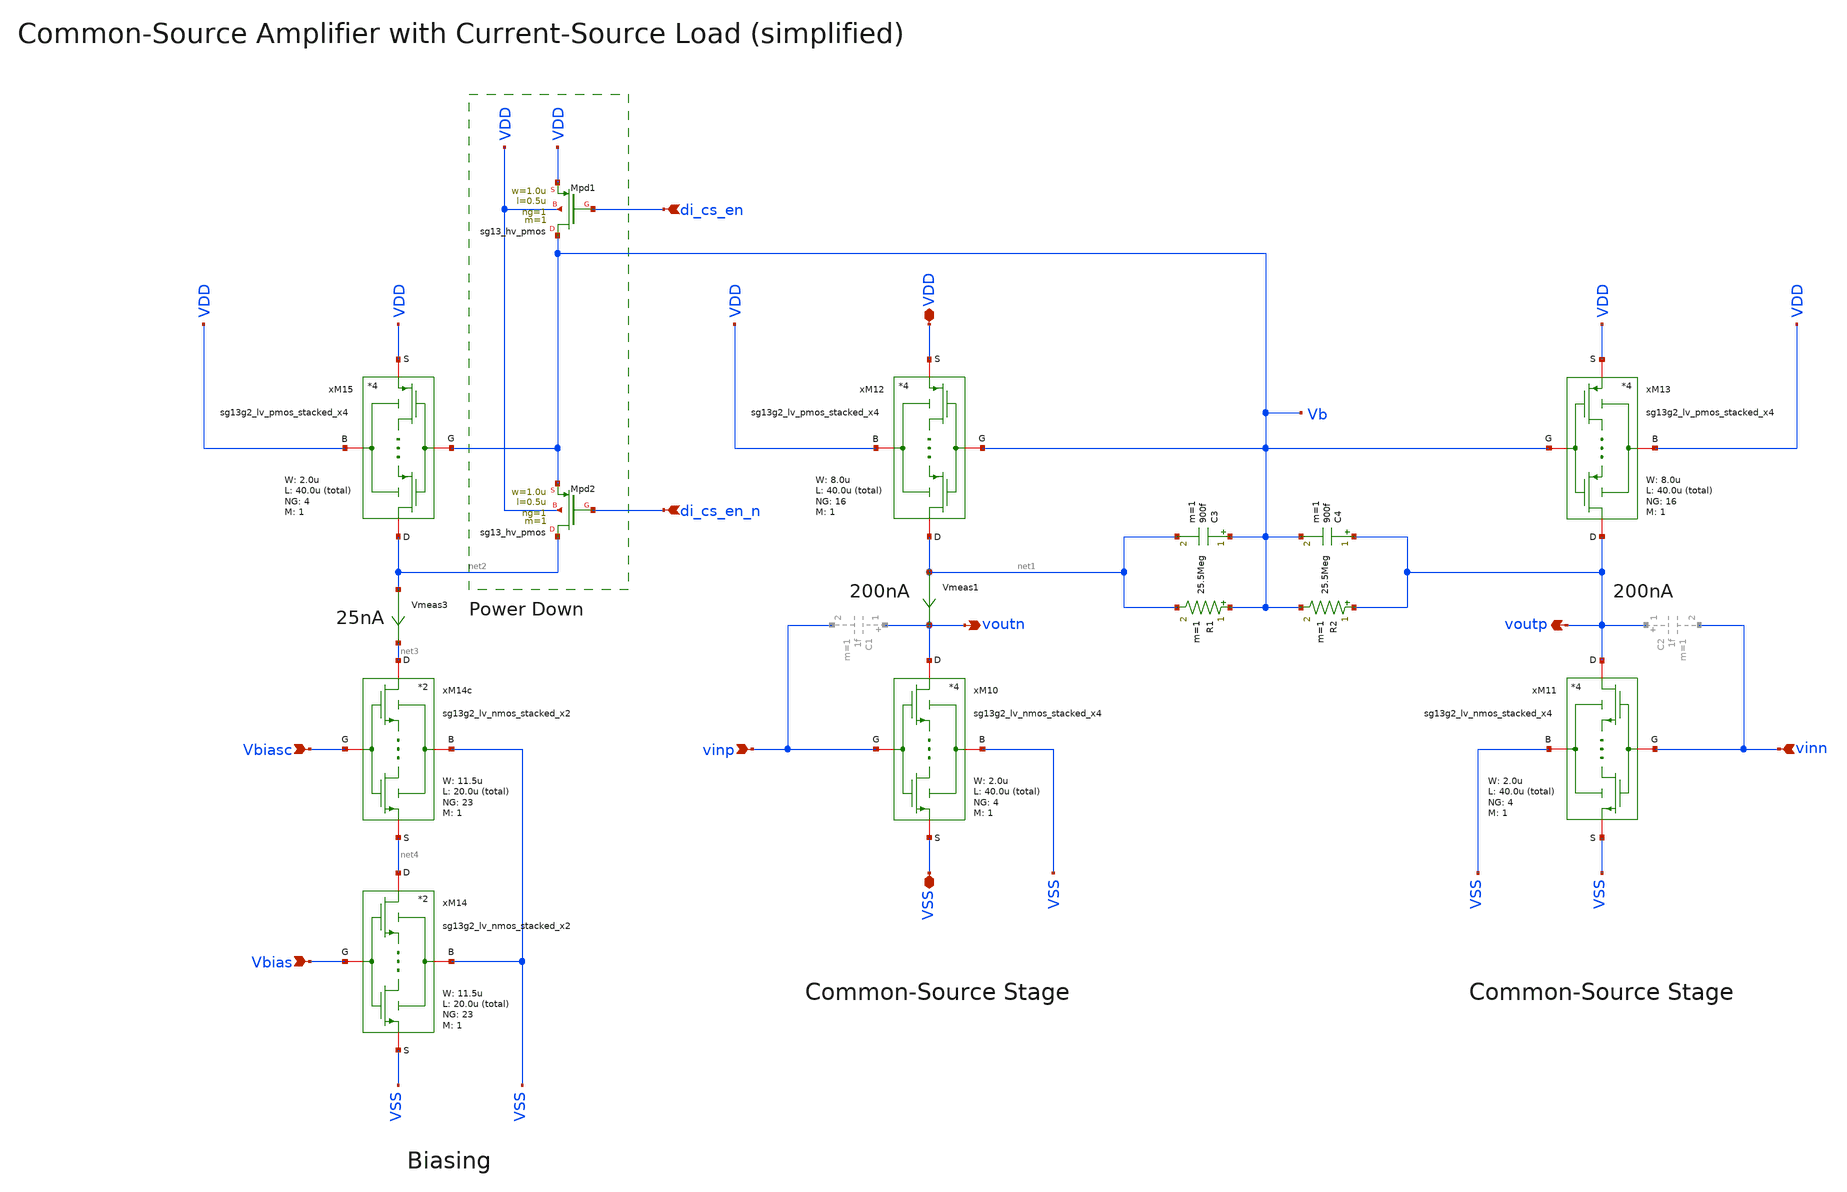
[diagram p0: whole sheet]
** sch_path: SG13G2_ATBS-ADC-main/xschem/bio_amplifier/amplifier_core/common_source_amplifier/common_source_amplifier_simplified.sch
**.subckt common_source_amplifier_simplified vinp vinn voutp voutn VDD VSS di_cs_en di_cs_en_n Vbias
*+ Vbiasc
*.ipin vinp
*.ipin vinn
*.opin voutp
*.opin voutn
*.iopin VDD
*.iopin VSS
*.ipin di_cs_en
*.ipin di_cs_en_n
*.ipin Vbias
*.ipin Vbiasc
xM12 net1 Vb VDD VDD sg13g2_lv_pmos_stacked_x4 W_P=8.0u L_P=40.0u NG_P=16 M_P=1
xM10 voutn vinp VSS VSS sg13g2_lv_nmos_stacked_x4 W_N=2.0u L_N=40.0u NG_N=4 M_N=1
R1 Vb net1 25.5Meg m=1
C3 Vb net1 900f m=1
xM13 voutp Vb VDD VDD sg13g2_lv_pmos_stacked_x4 W_P=8.0u L_P=40.0u NG_P=16 M_P=1
xM11 voutp vinn VSS VSS sg13g2_lv_nmos_stacked_x4 W_N=2.0u L_N=40.0u NG_N=4 M_N=1
C4 voutp Vb 900f m=1
R2 voutp Vb 25.5Meg m=1
xM15 net2 Vb VDD VDD sg13g2_lv_pmos_stacked_x4 W_P=2.0u L_P=40.0u NG_P=4 M_P=1
Vmeas1 net1 voutn 0
.save i(vmeas1)
XMpd2 net2 di_cs_en_n Vb VDD sg13_hv_pmos w=1.0u l=0.5u ng=1 m=1 mm_ok=1
XMpd1 Vb di_cs_en VDD VDD sg13_hv_pmos w=1.0u l=0.5u ng=1 m=1 mm_ok=1
Vmeas3 net2 net3 0
.save i(vmeas3)
xM14c net3 Vbiasc VSS net4 sg13g2_lv_nmos_stacked_x2 W_N=11.5u L_N=20.0u NG_N=23 M_N=1
xM14 net4 Vbias VSS VSS sg13g2_lv_nmos_stacked_x2 W_N=11.5u L_N=20.0u NG_N=23 M_N=1
**.ends

* expanding   symbol:  stacked_transistors/sg13g2_lv_pmos_stacked/sg13g2_lv_pmos_stacked_x4.sym # of
*+ pins=4
** sym_path: SG13G2_ATBS-ADC-main/xschem/stacked_transistors/sg13g2_lv_pmos_stacked/sg13g2_lv_pmos_stacked_x4.sym
** sch_path: SG13G2_ATBS-ADC-main/xschem/stacked_transistors/sg13g2_lv_pmos_stacked/sg13g2_lv_pmos_stacked_x4.sch
.subckt sg13g2_lv_pmos_stacked_x4 D G B S  W_P=1.0u L_P=0.45u NG_P=1 M_P=1
*.iopin D
*.iopin S
*.iopin G
*.iopin B
XM1 net1 G S B sg13_lv_pmos w=W_P l=L_P/4 ng=NG_P m=M_P mm_ok=1
XM2 net3 G net1 B sg13_lv_pmos w=W_P l=L_P/4 ng=NG_P m=M_P mm_ok=1
XM3 net2 G net3 B sg13_lv_pmos w=W_P l=L_P/4 ng=NG_P m=M_P mm_ok=1
XM4 D G net2 B sg13_lv_pmos w=W_P l=L_P/4 ng=NG_P m=M_P mm_ok=1
.ends


* expanding   symbol:  stacked_transistors/sg13g2_lv_nmos_stacked/sg13g2_lv_nmos_stacked_x4.sym # of
*+ pins=4
** sym_path: SG13G2_ATBS-ADC-main/xschem/stacked_transistors/sg13g2_lv_nmos_stacked/sg13g2_lv_nmos_stacked_x4.sym
** sch_path: SG13G2_ATBS-ADC-main/xschem/stacked_transistors/sg13g2_lv_nmos_stacked/sg13g2_lv_nmos_stacked_x4.sch
.subckt sg13g2_lv_nmos_stacked_x4 D G B S  W_N=1.0u L_N=0.45u NG_N=1 M_N=1
*.iopin D
*.iopin S
*.iopin G
*.iopin B
XM1 net1 G S B sg13_lv_nmos w=W_N l=L_N/4 ng=NG_N m=M_N mm_ok=1
XM2 net3 G net1 B sg13_lv_nmos w=W_N l=L_N/4 ng=NG_N m=M_N mm_ok=1
XM3 net2 G net3 B sg13_lv_nmos w=W_N l=L_N/4 ng=NG_N m=M_N mm_ok=1
XM4 D G net2 B sg13_lv_nmos w=W_N l=L_N/4 ng=NG_N m=M_N mm_ok=1
.ends


* expanding   symbol:  stacked_transistors/sg13g2_lv_nmos_stacked/sg13g2_lv_nmos_stacked_x2.sym # of
*+ pins=4
** sym_path: SG13G2_ATBS-ADC-main/xschem/stacked_transistors/sg13g2_lv_nmos_stacked/sg13g2_lv_nmos_stacked_x2.sym
** sch_path: SG13G2_ATBS-ADC-main/xschem/stacked_transistors/sg13g2_lv_nmos_stacked/sg13g2_lv_nmos_stacked_x2.sch
.subckt sg13g2_lv_nmos_stacked_x2 D G B S  W_N=1.0u L_N=0.45u NG_N=1 M_N=1
*.iopin D
*.iopin S
*.iopin G
*.iopin B
XM1 net1 G S B sg13_lv_nmos w=W_N l=L_N/2 ng=NG_N m=M_N mm_ok=1
XM2 D G net1 B sg13_lv_nmos w=W_N l=L_N/2 ng=NG_N m=M_N mm_ok=1
.ends

.end
